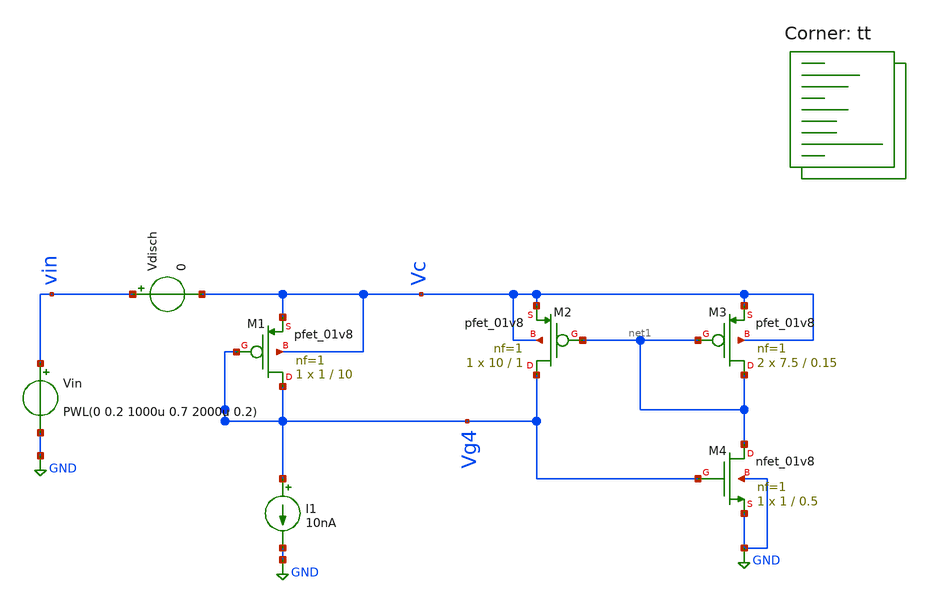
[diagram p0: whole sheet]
** sch_path: Neuron/ultralif/hysteresis_test.sch
**.subckt hysteresis_test
XM1 Vg4 Vg4 Vc Vc sky130_fd_pr__pfet_01v8 L=10 W=1 nf=1 ad='int((nf+1)/2) * W/nf * 0.29' as='int((nf+2)/2) * W/nf * 0.29'
+ pd='2*int((nf+1)/2) * (W/nf + 0.29)' ps='2*int((nf+2)/2) * (W/nf + 0.29)' nrd='0.29 / W' nrs='0.29 / W'
+ sa=0 sb=0 sd=0 mult=1 m=1
XM2 Vg4 net1 Vc Vc sky130_fd_pr__pfet_01v8 L=1 W=10 nf=1 ad='int((nf+1)/2) * W/nf * 0.29' as='int((nf+2)/2) * W/nf * 0.29'
+ pd='2*int((nf+1)/2) * (W/nf + 0.29)' ps='2*int((nf+2)/2) * (W/nf + 0.29)' nrd='0.29 / W' nrs='0.29 / W'
+ sa=0 sb=0 sd=0 mult=1 m=1
XM3 net1 net1 Vc Vc sky130_fd_pr__pfet_01v8 L=0.15 W=7.5 nf=1 ad='int((nf+1)/2) * W/nf * 0.29' as='int((nf+2)/2) * W/nf * 0.29'
+ pd='2*int((nf+1)/2) * (W/nf + 0.29)' ps='2*int((nf+2)/2) * (W/nf + 0.29)' nrd='0.29 / W' nrs='0.29 / W'
+ sa=0 sb=0 sd=0 mult=2 m=2
XM4 net1 Vg4 GND GND sky130_fd_pr__nfet_01v8 L=0.5 W=1 nf=1 ad='int((1 + 1)/2) * 1 / 1 * 0.29' as='int((1 + 2)/2) * 1 / 1 * 0.29'
+ pd='2*int((1 + 1)/2) * (1 / 1 + 0.29)' ps='2*int((1 + 2)/2) * (1 / 1 + 0.29)' nrd='0.29 / 1 ' nrs='0.29 / 1 '
+ sa=0 sb=0 sd=0 mult=1 m=1
I1 Vg4 GND 10nA
Vin vin GND PWL(0 0.2 1000u 0.7 2000u 0.2)
Vdisch vin Vc 0
**** begin user architecture code
.lib $::SKYWATER_MODELS/sky130.lib.spice tt
**** end user architecture code
**.ends
.GLOBAL GND
**** begin user architecture code

.options savecurrents
.tran 100n 2000u
*.dc Vin 0.2 0.7 0.01
.save all
.control
	run
	write prueba.raw
*plot all.Vout
.endc


**** end user architecture code
.end
